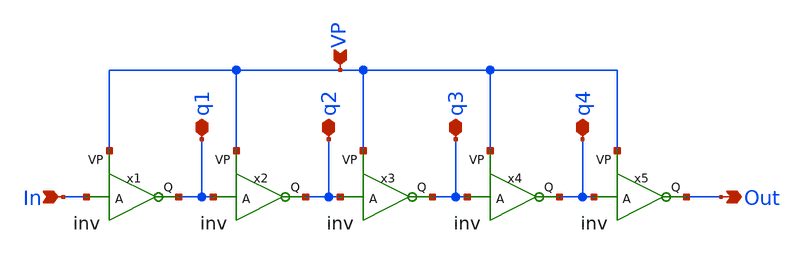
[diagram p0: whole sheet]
** sch_path: schemas/RING_OSC.sch
**.subckt RING_OSC Out In q1 q2 q3 q4 VP
*.opin Out
*.ipin In
*.iopin q1
*.iopin q2
*.iopin q3
*.iopin q4
*.ipin VP
x1 VP q1 In inv
x2 VP q2 q1 inv
x3 VP q3 q2 inv
x4 VP q4 q3 inv
x5 VP Out q4 inv
**.ends

* expanding   symbol:  /home/lxbtlr/DTILO/schemas/inv.sym # of pins=3
** sym_path: schemas/inv.sym
** sch_path: schemas/inv.sch
.subckt inv VP Q A
*.ipin A
*.opin Q
*.ipin VP
XM1 net1 A GND GND sky130_fd_pr__nfet_01v8 L={L} W={W}*6 nf=1 ad='int((nf+1)/2) * W/nf * 0.29' as='int((nf+2)/2) * W/nf * 0.29'
+ pd='2*int((nf+1)/2) * (W/nf + 0.29)' ps='2*int((nf+2)/2) * (W/nf + 0.29)' nrd='0.29 / W' nrs='0.29 / W'
+ sa=0 sb=0 sd=0 mult=1 m=1
XM2 net1 A VP VDD sky130_fd_pr__pfet_01v8 L={L} W={W}*20 nf=1 ad='int((nf+1)/2) * W/nf * 0.29' as='int((nf+2)/2) * W/nf * 0.29'
+ pd='2*int((nf+1)/2) * (W/nf + 0.29)' ps='2*int((nf+2)/2) * (W/nf + 0.29)' nrd='0.29 / W' nrs='0.29 / W'
+ sa=0 sb=0 sd=0 mult=1 m=1
XM3 net2 net1 GND GND sky130_fd_pr__nfet_01v8 L={L} W={W}*40 nf=1 ad='int((nf+1)/2) * W/nf * 0.29' as='int((nf+2)/2) * W/nf * 0.29'
+ pd='2*int((nf+1)/2) * (W/nf + 0.29)' ps='2*int((nf+2)/2) * (W/nf + 0.29)' nrd='0.29 / W' nrs='0.29 / W'
+ sa=0 sb=0 sd=0 mult=1 m=1
XM4 net2 net1 VDD VDD sky130_fd_pr__pfet_01v8 L={L} W={W}*10 nf=1 ad='int((nf+1)/2) * W/nf * 0.29' as='int((nf+2)/2) * W/nf * 0.29'
+ pd='2*int((nf+1)/2) * (W/nf + 0.29)' ps='2*int((nf+2)/2) * (W/nf + 0.29)' nrd='0.29 / W' nrs='0.29 / W'
+ sa=0 sb=0 sd=0 mult=1 m=1
XM5 Q net2 GND GND sky130_fd_pr__nfet_01v8 L={L} W={W}*6.5 nf=1 ad='int((nf+1)/2) * W/nf * 0.29' as='int((nf+2)/2) * W/nf * 0.29'
+ pd='2*int((nf+1)/2) * (W/nf + 0.29)' ps='2*int((nf+2)/2) * (W/nf + 0.29)' nrd='0.29 / W' nrs='0.29 / W'
+ sa=0 sb=0 sd=0 mult=1 m=1
XM6 Q net2 VDD VDD sky130_fd_pr__pfet_01v8 L={L} W={W}*30 nf=1 ad='int((nf+1)/2) * W/nf * 0.29' as='int((nf+2)/2) * W/nf * 0.29'
+ pd='2*int((nf+1)/2) * (W/nf + 0.29)' ps='2*int((nf+2)/2) * (W/nf + 0.29)' nrd='0.29 / W' nrs='0.29 / W'
+ sa=0 sb=0 sd=0 mult=1 m=1
C1 net1 GND 1f m=1
.ends

.GLOBAL GND
.GLOBAL VDD
.end
